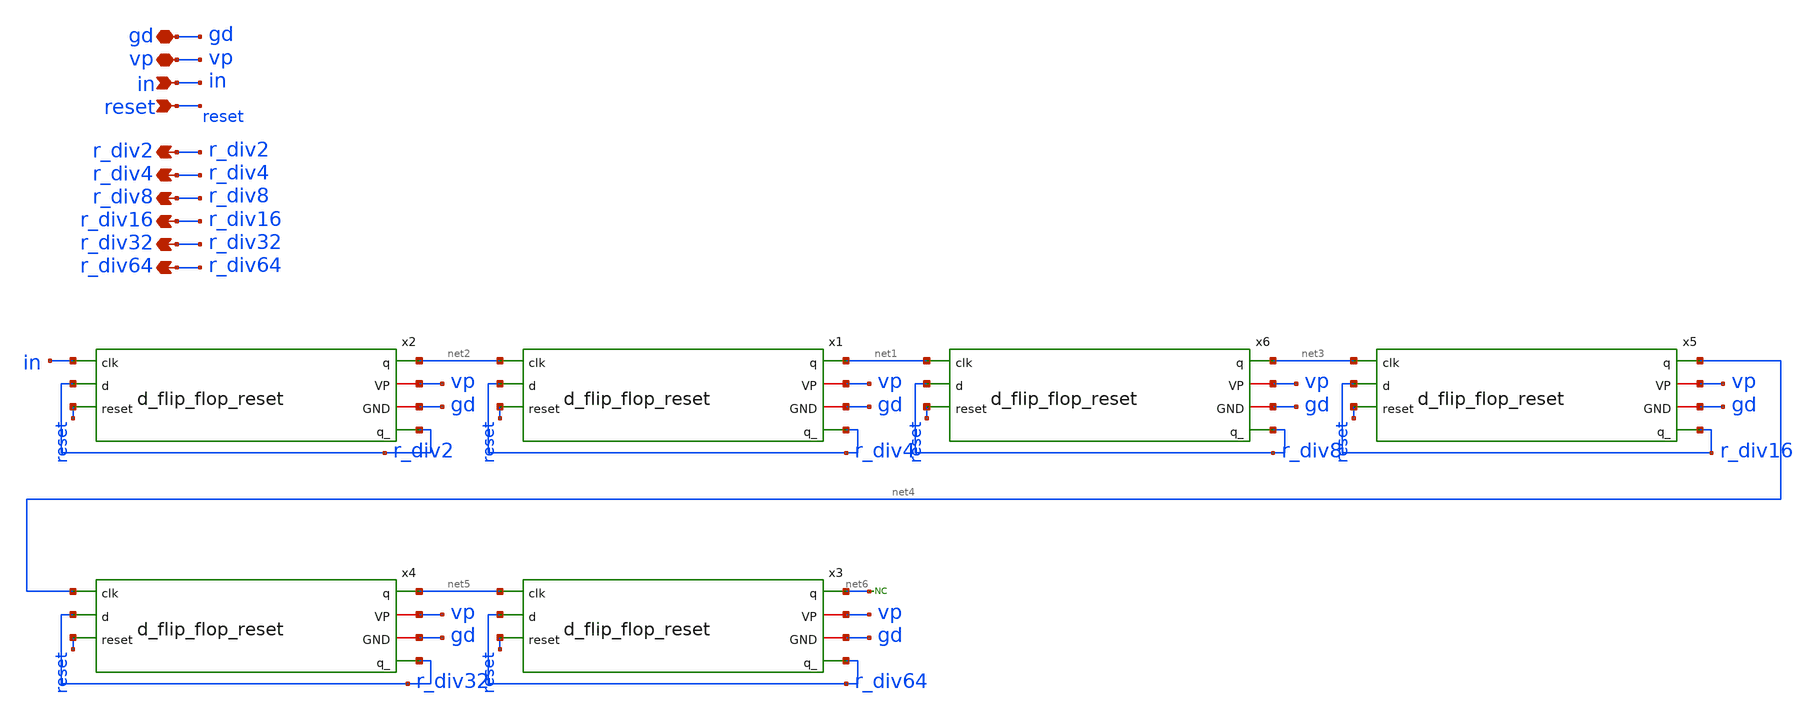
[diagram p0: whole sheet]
** sch_path: PLL0663-main/schematic/xschem/divider/div_with_reset.sch
**.subckt div_with_reset gd in vp r_div2 r_div4 r_div8 r_div16 r_div32 r_div64 reset
*.iopin gd
*.ipin in
*.iopin vp
*.opin r_div2
*.opin r_div4
*.opin r_div8
*.opin r_div16
*.opin r_div32
*.opin r_div64
*.ipin reset
x1 net1 vp gd r_div4 net2 r_div4 reset d_flip_flop_reset
x2 net2 vp gd r_div2 in r_div2 reset d_flip_flop_reset
x3 net6 vp gd r_div64 net5 r_div64 reset d_flip_flop_reset
x4 net5 vp gd r_div32 net4 r_div32 reset d_flip_flop_reset
x5 net4 vp gd r_div16 net3 r_div16 reset d_flip_flop_reset
x6 net3 vp gd r_div8 net1 r_div8 reset d_flip_flop_reset
* noconn #net6
**.ends
.end
